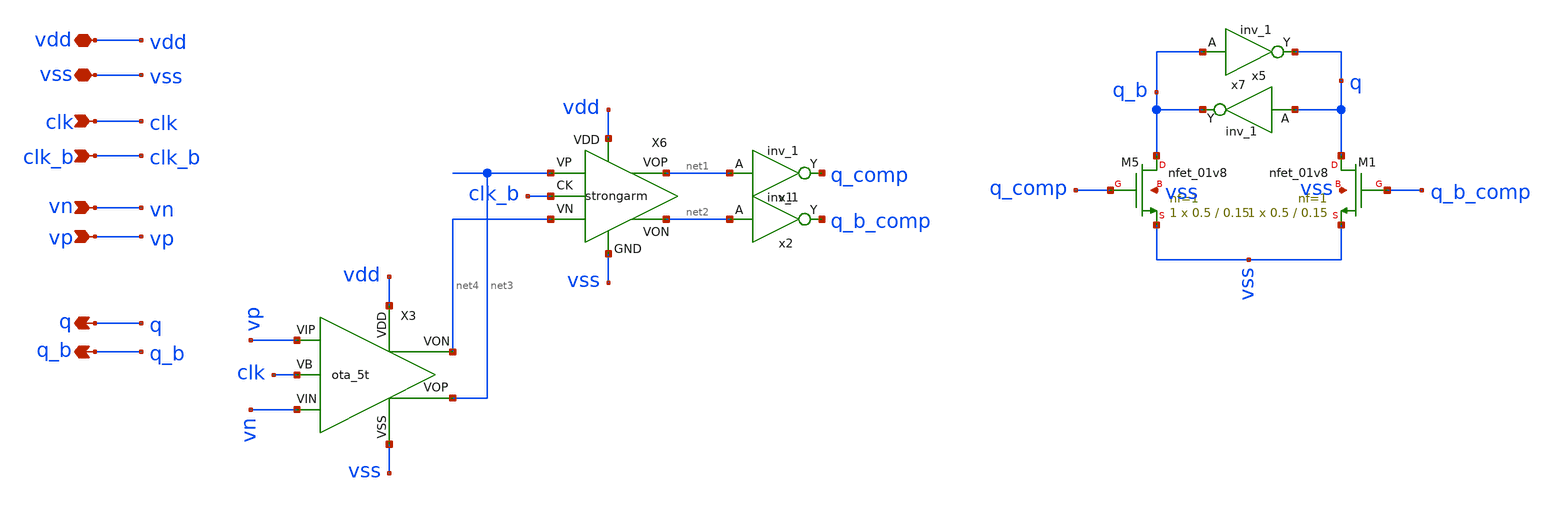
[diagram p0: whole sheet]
** sch_path: xschem/comparator/comparator.sch
**.subckt comparator vp vn vdd clk vss q q_b clk_b
*.ipin vp
*.ipin vn
*.iopin vdd
*.ipin clk
*.iopin vss
*.opin q
*.opin q_b
*.ipin clk_b
X6 net3 net4 vss net2 net1 vdd clk_b strongarm
XM5 q_b q_comp vss vss sky130_fd_pr__nfet_01v8 L=0.15 W=0.5 nf=1 ad='int((1 + 1)/2) * 0.5 / 1 * 0.29'
+ as='int((1 + 2)/2) * 0.5 / 1 * 0.29' pd='2*int((1 + 1)/2) * (0.5 / 1 + 0.29)' ps='2*int((1 + 2)/2) * (0.5 / 1 + 0.29)'
+ nrd='0.29 / 0.5 ' nrs='0.29 / 0.5 ' sa=0 sb=0 sd=0 mult=1 m=1
XM1 q q_b_comp vss vss sky130_fd_pr__nfet_01v8 L=0.15 W=0.5 nf=1 ad='int((1 + 1)/2) * 0.5 / 1 * 0.29'
+ as='int((1 + 2)/2) * 0.5 / 1 * 0.29' pd='2*int((1 + 1)/2) * (0.5 / 1 + 0.29)' ps='2*int((1 + 2)/2) * (0.5 / 1 + 0.29)'
+ nrd='0.29 / 0.5 ' nrs='0.29 / 0.5 ' sa=0 sb=0 sd=0 mult=1 m=1
x5 q_b vss vss vdd vdd q sky130_fd_sc_hd__inv_1
x7 q vss vss vdd vdd q_b sky130_fd_sc_hd__inv_1
x1 net1 vss vss vdd vdd q_comp sky130_fd_sc_hd__inv_1
x2 net2 vss vss vdd vdd q_b_comp sky130_fd_sc_hd__inv_1
X3 clk vn vp net3 vdd vss net4 ota_5t
**.ends

* expanding   symbol:  xschem/comparator/strongarm.sym # of pins=7
** sym_path: xschem/comparator/strongarm.sym
** sch_path: xschem/comparator/strongarm.sch
.subckt strongarm VP VN GND VON VOP VDD CK
*.iopin GND
*.ipin VP
*.opin VOP
*.opin VON
*.ipin VN
*.iopin VDD
*.ipin CK
XM2 net2 CK GND GND sky130_fd_pr__nfet_01v8 L=0.15 W=2 nf=2 ad='int((nf+1)/2) * W/nf * 0.29' as='int((nf+2)/2) * W/nf * 0.29'
+ pd='2*int((nf+1)/2) * (W/nf + 0.29)' ps='2*int((nf+2)/2) * (W/nf + 0.29)' nrd='0.29 / W' nrs='0.29 / W'
+ sa=0 sb=0 sd=0 mult=1 m=1
XM4 VON CK VDD VDD sky130_fd_pr__pfet_01v8 L=0.15 W=1 nf=1 ad='int((nf+1)/2) * W/nf * 0.29' as='int((nf+2)/2) * W/nf * 0.29'
+ pd='2*int((nf+1)/2) * (W/nf + 0.29)' ps='2*int((nf+2)/2) * (W/nf + 0.29)' nrd='0.29 / W' nrs='0.29 / W'
+ sa=0 sb=0 sd=0 mult=1 m=1
XM5 net1 CK VDD VDD sky130_fd_pr__pfet_01v8 L=0.15 W=1 nf=1 ad='int((nf+1)/2) * W/nf * 0.29' as='int((nf+2)/2) * W/nf * 0.29'
+ pd='2*int((nf+1)/2) * (W/nf + 0.29)' ps='2*int((nf+2)/2) * (W/nf + 0.29)' nrd='0.29 / W' nrs='0.29 / W'
+ sa=0 sb=0 sd=0 mult=1 m=1
XM8 net1 VP net2 GND sky130_fd_pr__nfet_01v8 L=0.15 W=2.5 nf=4 ad='int((nf+1)/2) * W/nf * 0.29' as='int((nf+2)/2) * W/nf * 0.29'
+ pd='2*int((nf+1)/2) * (W/nf + 0.29)' ps='2*int((nf+2)/2) * (W/nf + 0.29)' nrd='0.29 / W' nrs='0.29 / W'
+ sa=0 sb=0 sd=0 mult=1 m=1
XM9 VON VOP net1 GND sky130_fd_pr__nfet_01v8 L=0.15 W=2.5 nf=4 ad='int((nf+1)/2) * W/nf * 0.29' as='int((nf+2)/2) * W/nf * 0.29'
+ pd='2*int((nf+1)/2) * (W/nf + 0.29)' ps='2*int((nf+2)/2) * (W/nf + 0.29)' nrd='0.29 / W' nrs='0.29 / W'
+ sa=0 sb=0 sd=0 mult=1 m=1
XM11 VOP CK VDD VDD sky130_fd_pr__pfet_01v8 L=0.15 W=1 nf=1 ad='int((nf+1)/2) * W/nf * 0.29' as='int((nf+2)/2) * W/nf * 0.29'
+ pd='2*int((nf+1)/2) * (W/nf + 0.29)' ps='2*int((nf+2)/2) * (W/nf + 0.29)' nrd='0.29 / W' nrs='0.29 / W'
+ sa=0 sb=0 sd=0 mult=1 m=1
XM12 net3 CK VDD VDD sky130_fd_pr__pfet_01v8 L=0.15 W=1 nf=1 ad='int((nf+1)/2) * W/nf * 0.29' as='int((nf+2)/2) * W/nf * 0.29'
+ pd='2*int((nf+1)/2) * (W/nf + 0.29)' ps='2*int((nf+2)/2) * (W/nf + 0.29)' nrd='0.29 / W' nrs='0.29 / W'
+ sa=0 sb=0 sd=0 mult=1 m=1
XM13 net3 VN net2 GND sky130_fd_pr__nfet_01v8 L=0.15 W=2.5 nf=4 ad='int((nf+1)/2) * W/nf * 0.29' as='int((nf+2)/2) * W/nf * 0.29'
+ pd='2*int((nf+1)/2) * (W/nf + 0.29)' ps='2*int((nf+2)/2) * (W/nf + 0.29)' nrd='0.29 / W' nrs='0.29 / W'
+ sa=0 sb=0 sd=0 mult=1 m=1
XM14 VOP VON net3 GND sky130_fd_pr__nfet_01v8 L=0.15 W=10 nf=1 ad='int((nf+1)/2) * W/nf * 0.29' as='int((nf+2)/2) * W/nf * 0.29'
+ pd='2*int((nf+1)/2) * (W/nf + 0.29)' ps='2*int((nf+2)/2) * (W/nf + 0.29)' nrd='0.29 / W' nrs='0.29 / W'
+ sa=0 sb=0 sd=0 mult=1 m=1
XM15 VOP VON VDD VDD sky130_fd_pr__pfet_01v8 L=0.15 W=2.5 nf=1 ad='int((nf+1)/2) * W/nf * 0.29' as='int((nf+2)/2) * W/nf * 0.29'
+ pd='2*int((nf+1)/2) * (W/nf + 0.29)' ps='2*int((nf+2)/2) * (W/nf + 0.29)' nrd='0.29 / W' nrs='0.29 / W'
+ sa=0 sb=0 sd=0 mult=1 m=1
XM10 VON VOP VDD VDD sky130_fd_pr__pfet_01v8 L=0.15 W=2.5 nf=1 ad='int((nf+1)/2) * W/nf * 0.29' as='int((nf+2)/2) * W/nf * 0.29'
+ pd='2*int((nf+1)/2) * (W/nf + 0.29)' ps='2*int((nf+2)/2) * (W/nf + 0.29)' nrd='0.29 / W' nrs='0.29 / W'
+ sa=0 sb=0 sd=0 mult=1 m=1
.ends


* expanding   symbol:  xschem/preamp/ota_5t.sym # of pins=7
** sym_path: xschem/preamp/ota_5t.sym
** sch_path: xschem/preamp/ota_5t.sch
.subckt ota_5t VB VIN VIP VOP VDD VSS VON
*.iopin VDD
*.iopin VSS
*.opin VOP
*.ipin VIP
*.ipin VIN
*.ipin VB
*.opin VON
XM3 VON VIP net1 VSS sky130_fd_pr__nfet_01v8 L=1 W=5 nf=2 ad='int((2 + 1)/2) * 5 / 2 * 0.29' as='int((2 + 2)/2) * 5 / 2 * 0.29'
+ pd='2*int((2 + 1)/2) * (5 / 2 + 0.29)' ps='2*int((2 + 2)/2) * (5 / 2 + 0.29)' nrd='0.29 / 5 ' nrs='0.29 / 5 '
+ sa=0 sb=0 sd=0 mult=1 m=1
XM1 VOP VOP VDD VDD sky130_fd_pr__pfet_01v8 L=2.5 W=1.5 nf=2 ad='int((nf+1)/2) * W/nf * 0.29' as='int((nf+2)/2) * W/nf * 0.29'
+ pd='2*int((nf+1)/2) * (W/nf + 0.29)' ps='2*int((nf+2)/2) * (W/nf + 0.29)' nrd='0.29 / W' nrs='0.29 / W'
+ sa=0 sb=0 sd=0 mult=1 m=1
XM4 VOP VIN net1 VSS sky130_fd_pr__nfet_01v8 L=1 W=5 nf=2 ad='int((2 + 1)/2) * 5 / 2 * 0.29' as='int((2 + 2)/2) * 5 / 2 * 0.29'
+ pd='2*int((2 + 1)/2) * (5 / 2 + 0.29)' ps='2*int((2 + 2)/2) * (5 / 2 + 0.29)' nrd='0.29 / 5 ' nrs='0.29 / 5 '
+ sa=0 sb=0 sd=0 mult=1 m=1
XM5 net1 VB VSS VSS sky130_fd_pr__nfet_01v8 L=0.15 W=2 nf=1 ad='int((1 + 1)/2) * 2 / 1 * 0.29' as='int((1 + 2)/2) * 2 / 1 * 0.29'
+ pd='2*int((1 + 1)/2) * (2 / 1 + 0.29)' ps='2*int((1 + 2)/2) * (2 / 1 + 0.29)' nrd='0.29 / 2 ' nrs='0.29 / 2 '
+ sa=0 sb=0 sd=0 mult=1 m=1
XM8 VON VON VDD VDD sky130_fd_pr__pfet_01v8 L=2.5 W=1.5 nf=2 ad='int((nf+1)/2) * W/nf * 0.29' as='int((nf+2)/2) * W/nf * 0.29'
+ pd='2*int((nf+1)/2) * (W/nf + 0.29)' ps='2*int((nf+2)/2) * (W/nf + 0.29)' nrd='0.29 / W' nrs='0.29 / W'
+ sa=0 sb=0 sd=0 mult=1 m=1
.ends

.end
